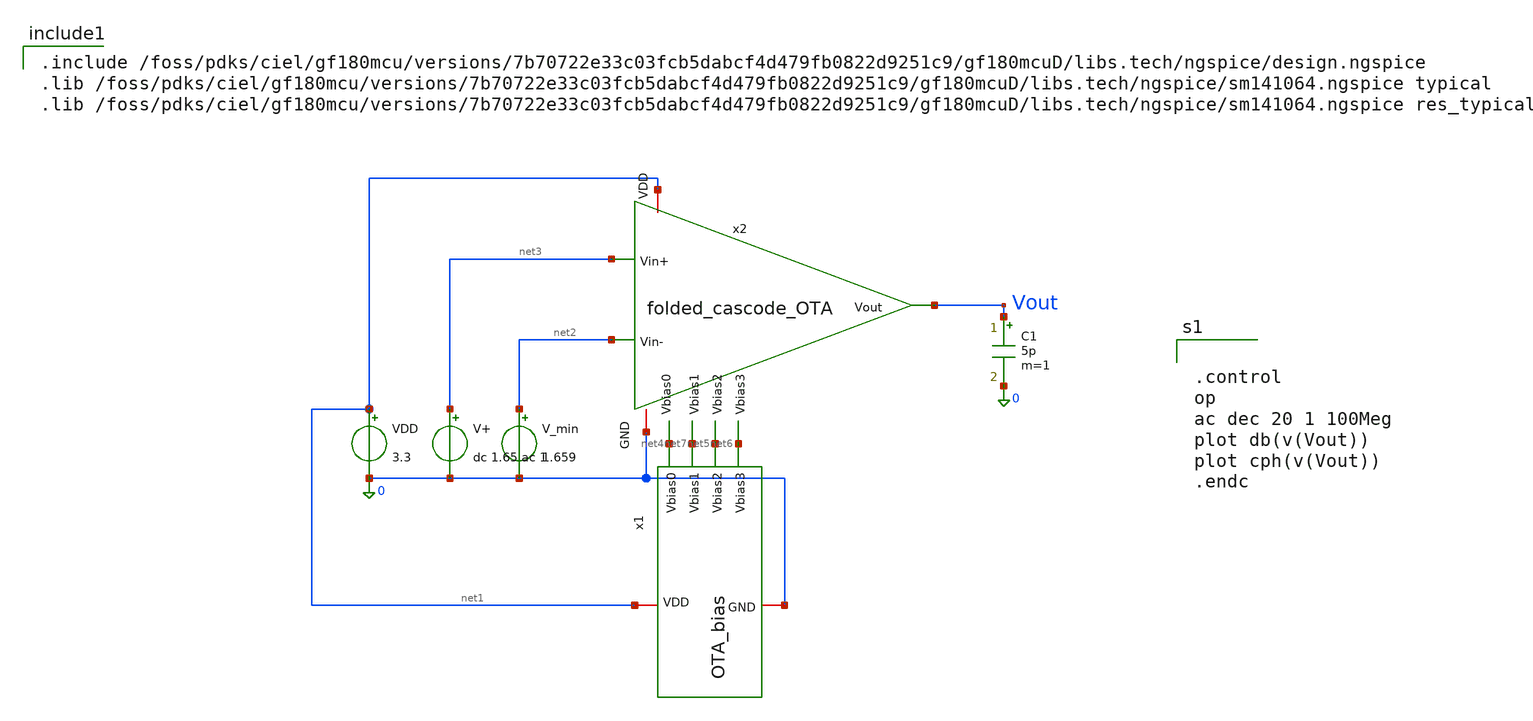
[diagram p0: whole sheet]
** sch_path: analog/tb_OTA.sch
**.subckt tb_OTA
x1 net1 net4 net5 net6 net7 0 OTA_bias cur_factor=1
x2 net1 net4 net3 net2 net6 net7 Vout net5 0 folded_cascode_OTA
VDD net1 0 3.3
C1 Vout 0 5p m=1
V_min net2 0 1.659
V+ net3 0 dc 1.65 ac 1
**** begin user architecture code


.control
op
ac dec 20 1 100Meg
plot db(v(Vout))
plot cph(v(Vout))
.endc



.include /foss/pdks/ciel/gf180mcu/versions/7b70722e33c03fcb5dabcf4d479fb0822d9251c9/gf180mcuD/libs.tech/ngspice/design.ngspice
.lib /foss/pdks/ciel/gf180mcu/versions/7b70722e33c03fcb5dabcf4d479fb0822d9251c9/gf180mcuD/libs.tech/ngspice/sm141064.ngspice typical
.lib /foss/pdks/ciel/gf180mcu/versions/7b70722e33c03fcb5dabcf4d479fb0822d9251c9/gf180mcuD/libs.tech/ngspice/sm141064.ngspice res_typical

**** end user architecture code
**.ends

* expanding   symbol:
*+  AURA-Event-Driven-Mixed-Signal-ASIC-for-Acoustic-Pattern-Detection/analog/OTA_bias.sym # of pins=6
** sym_path: analog/OTA_bias.sym
** sch_path: analog/OTA_bias.sch
.subckt OTA_bias VDD Vbias0 Vbias2 Vbias3 Vbias1 GND  cur_factor=1
*.iopin VDD
*.opin Vbias2
*.opin Vbias1
*.opin Vbias0
*.opin Vbias3
*.iopin GND
XM1 Vbias1 GND Vbias2 VDD pfet_03v3 L=4u W=5u nf=1 ad='int((nf+1)/2) * W/nf * 0.18u' as='int((nf+2)/2) * W/nf * 0.18u'
+ pd='2*int((nf+1)/2) * (W/nf + 0.18u)' ps='2*int((nf+2)/2) * (W/nf + 0.18u)' nrd='0.18u / W' nrs='0.18u / W'
+ sa=0 sb=0 sd=0 m=1
XM4 Vbias1 Vbias2 net1 GND nfet_03v3 L=4u W=1u nf=1 ad='int((nf+1)/2) * W/nf * 0.18u' as='int((nf+2)/2) * W/nf * 0.18u'
+ pd='2*int((nf+1)/2) * (W/nf + 0.18u)' ps='2*int((nf+2)/2) * (W/nf + 0.18u)' nrd='0.18u / W' nrs='0.18u / W'
+ sa=0 sb=0 sd=0 m=1
XM5 net1 Vbias1 GND GND nfet_03v3 L=4u W=1u nf=1 ad='int((nf+1)/2) * W/nf * 0.18u' as='int((nf+2)/2) * W/nf * 0.18u'
+ pd='2*int((nf+1)/2) * (W/nf + 0.18u)' ps='2*int((nf+2)/2) * (W/nf + 0.18u)' nrd='0.18u / W' nrs='0.18u / W'
+ sa=0 sb=0 sd=0 m=1
XM9 net2 Vbias3 Vbias0 VDD pfet_03v3 L=4u W=5u nf=1 ad='int((nf+1)/2) * W/nf * 0.18u' as='int((nf+2)/2) * W/nf * 0.18u'
+ pd='2*int((nf+1)/2) * (W/nf + 0.18u)' ps='2*int((nf+2)/2) * (W/nf + 0.18u)' nrd='0.18u / W' nrs='0.18u / W'
+ sa=0 sb=0 sd=0 m=1
XM10 VDD Vbias0 net2 VDD pfet_03v3 L=4u W=5u nf=1 ad='int((nf+1)/2) * W/nf * 0.18u' as='int((nf+2)/2) * W/nf * 0.18u'
+ pd='2*int((nf+1)/2) * (W/nf + 0.18u)' ps='2*int((nf+2)/2) * (W/nf + 0.18u)' nrd='0.18u / W' nrs='0.18u / W'
+ sa=0 sb=0 sd=0 m=1
XM6 Vbias3 VDD Vbias0 GND nfet_03v3 L=4u W=10u nf=1 ad='int((nf+1)/2) * W/nf * 0.18u' as='int((nf+2)/2) * W/nf * 0.18u'
+ pd='2*int((nf+1)/2) * (W/nf + 0.18u)' ps='2*int((nf+2)/2) * (W/nf + 0.18u)' nrd='0.18u / W' nrs='0.18u / W'
+ sa=0 sb=0 sd=0 m=1
x1 VDD net3 net4 GND beta_multiplier_reference cur_factor={cur_factor}
XM2 Vbias2 net3 VDD VDD pfet_03v3 L=4u W=10u nf=1 ad='int((nf+1)/2) * W/nf * 0.18u' as='int((nf+2)/2) * W/nf * 0.18u'
+ pd='2*int((nf+1)/2) * (W/nf + 0.18u)' ps='2*int((nf+2)/2) * (W/nf + 0.18u)' nrd='0.18u / W' nrs='0.18u / W'
+ sa=0 sb=0 sd=0 m=1
XM3 GND net4 Vbias3 GND nfet_03v3 L=4u W=10u nf=1 ad='int((nf+1)/2) * W/nf * 0.18u' as='int((nf+2)/2) * W/nf * 0.18u'
+ pd='2*int((nf+1)/2) * (W/nf + 0.18u)' ps='2*int((nf+2)/2) * (W/nf + 0.18u)' nrd='0.18u / W' nrs='0.18u / W'
+ sa=0 sb=0 sd=0 m=1
.ends


* expanding   symbol:
*+  AURA-Event-Driven-Mixed-Signal-ASIC-for-Acoustic-Pattern-Detection/analog/folded_cascode_OTA.sym # of pins=9
** sym_path: analog/folded_cascode_OTA.sym
** sch_path: analog/folded_cascode_OTA.sch
.subckt folded_cascode_OTA VDD Vbias0 Vin+ Vin- Vbias3 Vbias1 Vout Vbias2 GND
*.iopin VDD
*.ipin Vbias0
*.ipin Vin+
*.ipin Vin-
*.ipin Vbias1
*.opin Vout
*.ipin Vbias3
*.ipin Vbias2
*.iopin GND
XM1 net1 Vbias0 VDD VDD pfet_03v3 L=4u W=5u nf=2 ad='int((nf+1)/2) * W/nf * 0.18u' as='int((nf+2)/2) * W/nf * 0.18u'
+ pd='2*int((nf+1)/2) * (W/nf + 0.18u)' ps='2*int((nf+2)/2) * (W/nf + 0.18u)' nrd='0.18u / W' nrs='0.18u / W'
+ sa=0 sb=0 sd=0 m=1
XM2 net6 Vin+ net1 VDD pfet_03v3 L=1u W=2u nf=9 ad='int((nf+1)/2) * W/nf * 0.18u' as='int((nf+2)/2) * W/nf * 0.18u'
+ pd='2*int((nf+1)/2) * (W/nf + 0.18u)' ps='2*int((nf+2)/2) * (W/nf + 0.18u)' nrd='0.18u / W' nrs='0.18u / W'
+ sa=0 sb=0 sd=0 m=1
XM3 net7 Vin- net1 VDD pfet_03v3 L=1u W=2u nf=9 ad='int((nf+1)/2) * W/nf * 0.18u' as='int((nf+2)/2) * W/nf * 0.18u'
+ pd='2*int((nf+1)/2) * (W/nf + 0.18u)' ps='2*int((nf+2)/2) * (W/nf + 0.18u)' nrd='0.18u / W' nrs='0.18u / W'
+ sa=0 sb=0 sd=0 m=1
XM4 net2 Vin+ net1 VDD pfet_03v3 L=1u W=2u nf=1 ad='int((nf+1)/2) * W/nf * 0.18u' as='int((nf+2)/2) * W/nf * 0.18u'
+ pd='2*int((nf+1)/2) * (W/nf + 0.18u)' ps='2*int((nf+2)/2) * (W/nf + 0.18u)' nrd='0.18u / W' nrs='0.18u / W'
+ sa=0 sb=0 sd=0 m=1
XM5 net3 Vin- net1 VDD pfet_03v3 L=1u W=2u nf=1 ad='int((nf+1)/2) * W/nf * 0.18u' as='int((nf+2)/2) * W/nf * 0.18u'
+ pd='2*int((nf+1)/2) * (W/nf + 0.18u)' ps='2*int((nf+2)/2) * (W/nf + 0.18u)' nrd='0.18u / W' nrs='0.18u / W'
+ sa=0 sb=0 sd=0 m=1
XM6 net2 Vbias2 net5 0 nfet_03v3 L=1u W=2u nf=1 ad='int((nf+1)/2) * W/nf * 0.18u' as='int((nf+2)/2) * W/nf * 0.18u'
+ pd='2*int((nf+1)/2) * (W/nf + 0.18u)' ps='2*int((nf+2)/2) * (W/nf + 0.18u)' nrd='0.18u / W' nrs='0.18u / W'
+ sa=0 sb=0 sd=0 m=1
XM7 net3 Vbias2 net4 0 nfet_03v3 L=1u W=2u nf=1 ad='int((nf+1)/2) * W/nf * 0.18u' as='int((nf+2)/2) * W/nf * 0.18u'
+ pd='2*int((nf+1)/2) * (W/nf + 0.18u)' ps='2*int((nf+2)/2) * (W/nf + 0.18u)' nrd='0.18u / W' nrs='0.18u / W'
+ sa=0 sb=0 sd=0 m=1
XM8 net5 net2 GND GND nfet_03v3 L=4u W=1u nf=1 ad='int((nf+1)/2) * W/nf * 0.18u' as='int((nf+2)/2) * W/nf * 0.18u'
+ pd='2*int((nf+1)/2) * (W/nf + 0.18u)' ps='2*int((nf+2)/2) * (W/nf + 0.18u)' nrd='0.18u / W' nrs='0.18u / W'
+ sa=0 sb=0 sd=0 m=1
XM9 net6 net3 GND GND nfet_03v3 L=4u W=1u nf=1 ad='int((nf+1)/2) * W/nf * 0.18u' as='int((nf+2)/2) * W/nf * 0.18u'
+ pd='2*int((nf+1)/2) * (W/nf + 0.18u)' ps='2*int((nf+2)/2) * (W/nf + 0.18u)' nrd='0.18u / W' nrs='0.18u / W'
+ sa=0 sb=0 sd=0 m=1
XM10 net4 net3 GND GND nfet_03v3 L=4u W=1u nf=1 ad='int((nf+1)/2) * W/nf * 0.18u' as='int((nf+2)/2) * W/nf * 0.18u'
+ pd='2*int((nf+1)/2) * (W/nf + 0.18u)' ps='2*int((nf+2)/2) * (W/nf + 0.18u)' nrd='0.18u / W' nrs='0.18u / W'
+ sa=0 sb=0 sd=0 m=1
XM11 net7 net2 GND GND nfet_03v3 L=4u W=1u nf=1 ad='int((nf+1)/2) * W/nf * 0.18u' as='int((nf+2)/2) * W/nf * 0.18u'
+ pd='2*int((nf+1)/2) * (W/nf + 0.18u)' ps='2*int((nf+2)/2) * (W/nf + 0.18u)' nrd='0.18u / W' nrs='0.18u / W'
+ sa=0 sb=0 sd=0 m=1
XM12 net9 net10 VDD VDD pfet_03v3 L=4u W=5u nf=1 ad='int((nf+1)/2) * W/nf * 0.18u' as='int((nf+2)/2) * W/nf * 0.18u'
+ pd='2*int((nf+1)/2) * (W/nf + 0.18u)' ps='2*int((nf+2)/2) * (W/nf + 0.18u)' nrd='0.18u / W' nrs='0.18u / W'
+ sa=0 sb=0 sd=0 m=1
XM13 net8 net10 VDD VDD pfet_03v3 L=4u W=5u nf=1 ad='int((nf+1)/2) * W/nf * 0.18u' as='int((nf+2)/2) * W/nf * 0.18u'
+ pd='2*int((nf+1)/2) * (W/nf + 0.18u)' ps='2*int((nf+2)/2) * (W/nf + 0.18u)' nrd='0.18u / W' nrs='0.18u / W'
+ sa=0 sb=0 sd=0 m=1
XM14 Vout Vbias3 net9 VDD pfet_03v3 L=4u W=5u nf=1 ad='int((nf+1)/2) * W/nf * 0.18u' as='int((nf+2)/2) * W/nf * 0.18u'
+ pd='2*int((nf+1)/2) * (W/nf + 0.18u)' ps='2*int((nf+2)/2) * (W/nf + 0.18u)' nrd='0.18u / W' nrs='0.18u / W'
+ sa=0 sb=0 sd=0 m=1
XM15 net10 Vbias3 net8 VDD pfet_03v3 L=4u W=5u nf=1 ad='int((nf+1)/2) * W/nf * 0.18u' as='int((nf+2)/2) * W/nf * 0.18u'
+ pd='2*int((nf+1)/2) * (W/nf + 0.18u)' ps='2*int((nf+2)/2) * (W/nf + 0.18u)' nrd='0.18u / W' nrs='0.18u / W'
+ sa=0 sb=0 sd=0 m=1
XM16 Vout Vbias1 net7 0 nfet_03v3 L=4u W=1u nf=1 ad='int((nf+1)/2) * W/nf * 0.18u' as='int((nf+2)/2) * W/nf * 0.18u'
+ pd='2*int((nf+1)/2) * (W/nf + 0.18u)' ps='2*int((nf+2)/2) * (W/nf + 0.18u)' nrd='0.18u / W' nrs='0.18u / W'
+ sa=0 sb=0 sd=0 m=1
XM17 net10 Vbias1 net6 0 nfet_03v3 L=4u W=1u nf=1 ad='int((nf+1)/2) * W/nf * 0.18u' as='int((nf+2)/2) * W/nf * 0.18u'
+ pd='2*int((nf+1)/2) * (W/nf + 0.18u)' ps='2*int((nf+2)/2) * (W/nf + 0.18u)' nrd='0.18u / W' nrs='0.18u / W'
+ sa=0 sb=0 sd=0 m=1
.ends


* expanding   symbol:
*+  AURA-Event-Driven-Mixed-Signal-ASIC-for-Acoustic-Pattern-Detection/analog/beta_multiplier_reference.sym # of pins=4
** sym_path: analog/beta_multiplier_reference.sym
** sch_path: analog/beta_multiplier_reference.sch
.subckt beta_multiplier_reference VDD VbiasP VbiasN GND  length=410u
*.iopin VDD
*.iopin GND
*.opin VbiasP
*.opin VbiasN
XM2 VbiasN VbiasP VDD VDD pfet_03v3 L=4u W=2u nf=1 ad='int((nf+1)/2) * W/nf * 0.18u' as='int((nf+2)/2) * W/nf * 0.18u'
+ pd='2*int((nf+1)/2) * (W/nf + 0.18u)' ps='2*int((nf+2)/2) * (W/nf + 0.18u)' nrd='0.18u / W' nrs='0.18u / W'
+ sa=0 sb=0 sd=0 m=1
XM3 net2 VbiasP VDD VDD pfet_03v3 L=4u W=2u nf=1 ad='int((nf+1)/2) * W/nf * 0.18u' as='int((nf+2)/2) * W/nf * 0.18u'
+ pd='2*int((nf+1)/2) * (W/nf + 0.18u)' ps='2*int((nf+2)/2) * (W/nf + 0.18u)' nrd='0.18u / W' nrs='0.18u / W'
+ sa=0 sb=0 sd=0 m=1
XM6 VbiasN VbiasN GND GND nfet_03v3 L=4u W=10u nf=1 ad='int((nf+1)/2) * W/nf * 0.18u' as='int((nf+2)/2) * W/nf * 0.18u'
+ pd='2*int((nf+1)/2) * (W/nf + 0.18u)' ps='2*int((nf+2)/2) * (W/nf + 0.18u)' nrd='0.18u / W' nrs='0.18u / W'
+ sa=0 sb=0 sd=0 m=1
XM7 net2 VbiasN net1 GND nfet_03v3 L=4u W=10u nf=1 ad='int((nf+1)/2) * W/nf * 0.18u' as='int((nf+2)/2) * W/nf * 0.18u'
+ pd='2*int((nf+1)/2) * (W/nf + 0.18u)' ps='2*int((nf+2)/2) * (W/nf + 0.18u)' nrd='0.18u / W' nrs='0.18u / W'
+ sa=0 sb=0 sd=0 m=4
x1 VDD VbiasP net2 VbiasN VbiasN GND diff_amp
XM1 net4 net4 VDD VDD pfet_03v3 L=40u W=0.22u nf=1 ad='int((nf+1)/2) * W/nf * 0.18u' as='int((nf+2)/2) * W/nf * 0.18u'
+ pd='2*int((nf+1)/2) * (W/nf + 0.18u)' ps='2*int((nf+2)/2) * (W/nf + 0.18u)' nrd='0.18u / W' nrs='0.18u / W'
+ sa=0 sb=0 sd=0 m=1
XM4 VbiasP net3 VbiasN GND nfet_03v3 L=1u W=1u nf=1 ad='int((nf+1)/2) * W/nf * 0.18u' as='int((nf+2)/2) * W/nf * 0.18u'
+ pd='2*int((nf+1)/2) * (W/nf + 0.18u)' ps='2*int((nf+2)/2) * (W/nf + 0.18u)' nrd='0.18u / W' nrs='0.18u / W'
+ sa=0 sb=0 sd=0 m=1
XM5 net3 VbiasN GND GND nfet_03v3 L=10u W=1u nf=1 ad='int((nf+1)/2) * W/nf * 0.18u' as='int((nf+2)/2) * W/nf * 0.18u'
+ pd='2*int((nf+1)/2) * (W/nf + 0.18u)' ps='2*int((nf+2)/2) * (W/nf + 0.18u)' nrd='0.18u / W' nrs='0.18u / W'
+ sa=0 sb=0 sd=0 m=1
XM8 net5 net5 net4 VDD pfet_03v3 L=40u W=0.22u nf=1 ad='int((nf+1)/2) * W/nf * 0.18u' as='int((nf+2)/2) * W/nf * 0.18u'
+ pd='2*int((nf+1)/2) * (W/nf + 0.18u)' ps='2*int((nf+2)/2) * (W/nf + 0.18u)' nrd='0.18u / W' nrs='0.18u / W'
+ sa=0 sb=0 sd=0 m=1
XM9 net3 net5 net5 VDD pfet_03v3 L=40u W=0.22u nf=1 ad='int((nf+1)/2) * W/nf * 0.18u' as='int((nf+2)/2) * W/nf * 0.18u'
+ pd='2*int((nf+1)/2) * (W/nf + 0.18u)' ps='2*int((nf+2)/2) * (W/nf + 0.18u)' nrd='0.18u / W' nrs='0.18u / W'
+ sa=0 sb=0 sd=0 m=1
XR2 GND net1 GND ppolyf_u_2k r_width=2u r_length={length} m=1
.ends


* expanding   symbol:  AURA/diff_amp.sym # of pins=6
** sym_path: analog/diff_amp.sym
** sch_path: analog/diff_amp.sch
.subckt diff_amp VDD Vo V+ V- Vbias VSS
*.iopin VDD
*.iopin VSS
*.ipin V+
*.ipin V-
*.opin Vo
*.ipin Vbias
XM1 net1 V+ net2 VSS nfet_03v3 L=0.28u W=0.22u nf=1 ad='int((nf+1)/2) * W/nf * 0.18u' as='int((nf+2)/2) * W/nf * 0.18u'
+ pd='2*int((nf+1)/2) * (W/nf + 0.18u)' ps='2*int((nf+2)/2) * (W/nf + 0.18u)' nrd='0.18u / W' nrs='0.18u / W'
+ sa=0 sb=0 sd=0 m=1
XM2 net2 Vbias VSS VSS nfet_03v3 L=0.28u W=0.22u nf=1 ad='int((nf+1)/2) * W/nf * 0.18u' as='int((nf+2)/2) * W/nf * 0.18u'
+ pd='2*int((nf+1)/2) * (W/nf + 0.18u)' ps='2*int((nf+2)/2) * (W/nf + 0.18u)' nrd='0.18u / W' nrs='0.18u / W'
+ sa=0 sb=0 sd=0 m=1
XM3 Vo V- net2 VSS nfet_03v3 L=0.28u W=0.22u nf=1 ad='int((nf+1)/2) * W/nf * 0.18u' as='int((nf+2)/2) * W/nf * 0.18u'
+ pd='2*int((nf+1)/2) * (W/nf + 0.18u)' ps='2*int((nf+2)/2) * (W/nf + 0.18u)' nrd='0.18u / W' nrs='0.18u / W'
+ sa=0 sb=0 sd=0 m=1
XM4 Vo net1 VDD VDD pfet_03v3 L=0.28u W=0.22u nf=1 ad='int((nf+1)/2) * W/nf * 0.18u' as='int((nf+2)/2) * W/nf * 0.18u'
+ pd='2*int((nf+1)/2) * (W/nf + 0.18u)' ps='2*int((nf+2)/2) * (W/nf + 0.18u)' nrd='0.18u / W' nrs='0.18u / W'
+ sa=0 sb=0 sd=0 m=1
XM5 net1 net1 VDD VDD pfet_03v3 L=0.28u W=0.22u nf=1 ad='int((nf+1)/2) * W/nf * 0.18u' as='int((nf+2)/2) * W/nf * 0.18u'
+ pd='2*int((nf+1)/2) * (W/nf + 0.18u)' ps='2*int((nf+2)/2) * (W/nf + 0.18u)' nrd='0.18u / W' nrs='0.18u / W'
+ sa=0 sb=0 sd=0 m=1
.ends

.end
